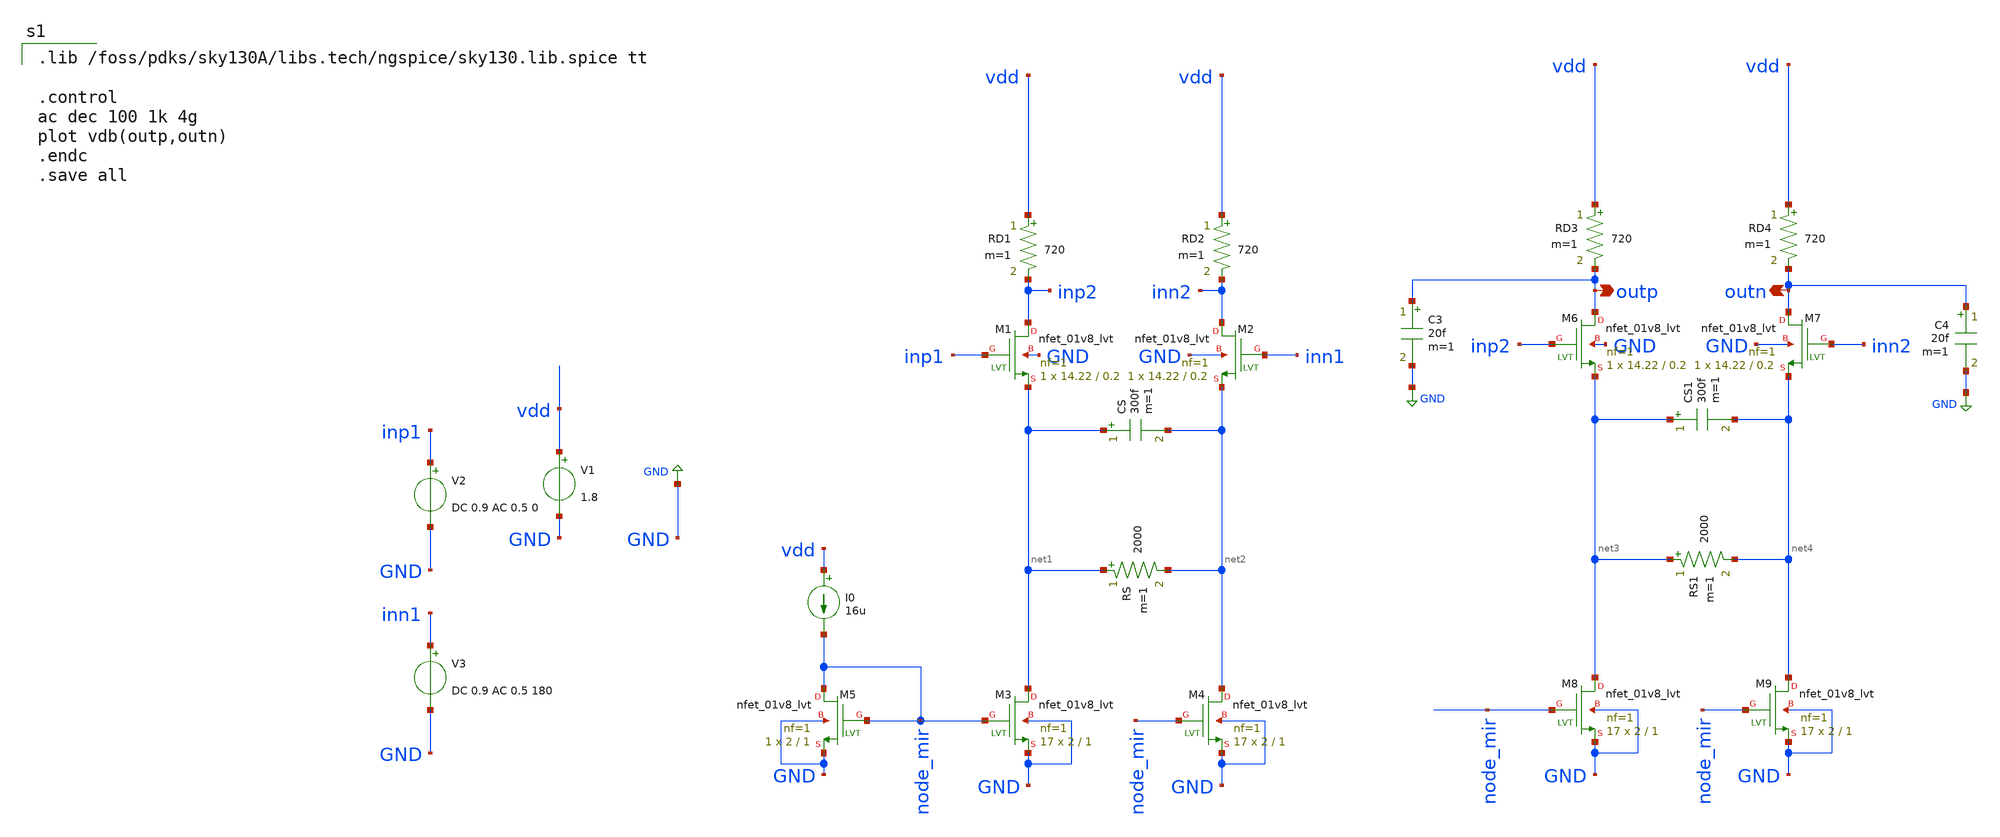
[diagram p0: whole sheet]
** sch_path: CTLE/ctle_two_stage.sch
**.subckt ctle_two_stage outp outn
*.opin outp
*.opin outn
V1 vdd GND 1.8
V2 inp1 GND DC 0.9 AC 0.5 0
V3 inn1 GND DC 0.9 AC 0.5 180
XM1 inp2 inp1 net1 GND sky130_fd_pr__nfet_01v8_lvt L=0.2 W=14.22 nf=1 ad='int((nf+1)/2) * W/nf * 0.29'
+ as='int((nf+2)/2) * W/nf * 0.29' pd='2*int((nf+1)/2) * (W/nf + 0.29)' ps='2*int((nf+2)/2) * (W/nf + 0.29)'
+ nrd='0.29 / W' nrs='0.29 / W' sa=0 sb=0 sd=0 mult=1 m=1
XM2 inn2 inn1 net2 GND sky130_fd_pr__nfet_01v8_lvt L=0.2 W=14.22 nf=1 ad='int((nf+1)/2) * W/nf * 0.29'
+ as='int((nf+2)/2) * W/nf * 0.29' pd='2*int((nf+1)/2) * (W/nf + 0.29)' ps='2*int((nf+2)/2) * (W/nf + 0.29)'
+ nrd='0.29 / W' nrs='0.29 / W' sa=0 sb=0 sd=0 mult=1 m=1
I0 vdd node_mir 16u
XM3 net1 node_mir GND GND sky130_fd_pr__nfet_01v8_lvt L=1 W=2 nf=1 ad='int((nf+1)/2) * W/nf * 0.29' as='int((nf+2)/2) * W/nf * 0.29'
+ pd='2*int((nf+1)/2) * (W/nf + 0.29)' ps='2*int((nf+2)/2) * (W/nf + 0.29)' nrd='0.29 / W' nrs='0.29 / W'
+ sa=0 sb=0 sd=0 mult=17 m=17
XM4 net2 node_mir GND GND sky130_fd_pr__nfet_01v8_lvt L=1 W=2 nf=1 ad='int((nf+1)/2) * W/nf * 0.29' as='int((nf+2)/2) * W/nf * 0.29'
+ pd='2*int((nf+1)/2) * (W/nf + 0.29)' ps='2*int((nf+2)/2) * (W/nf + 0.29)' nrd='0.29 / W' nrs='0.29 / W'
+ sa=0 sb=0 sd=0 mult=17 m=17
XM5 node_mir node_mir GND GND sky130_fd_pr__nfet_01v8_lvt L=1 W=2 nf=1 ad='int((nf+1)/2) * W/nf * 0.29'
+ as='int((nf+2)/2) * W/nf * 0.29' pd='2*int((nf+1)/2) * (W/nf + 0.29)' ps='2*int((nf+2)/2) * (W/nf + 0.29)'
+ nrd='0.29 / W' nrs='0.29 / W' sa=0 sb=0 sd=0 mult=1 m=1
RD1 vdd inp2 720 m=1
RD2 vdd inn2 720 m=1
CS net1 net2 300f m=1
RS net1 net2 2000 m=1
XM6 outp inp2 net3 GND sky130_fd_pr__nfet_01v8_lvt L=0.2 W=14.22 nf=1 ad='int((nf+1)/2) * W/nf * 0.29'
+ as='int((nf+2)/2) * W/nf * 0.29' pd='2*int((nf+1)/2) * (W/nf + 0.29)' ps='2*int((nf+2)/2) * (W/nf + 0.29)'
+ nrd='0.29 / W' nrs='0.29 / W' sa=0 sb=0 sd=0 mult=1 m=1
XM7 outn inn2 net4 GND sky130_fd_pr__nfet_01v8_lvt L=0.2 W=14.22 nf=1 ad='int((nf+1)/2) * W/nf * 0.29'
+ as='int((nf+2)/2) * W/nf * 0.29' pd='2*int((nf+1)/2) * (W/nf + 0.29)' ps='2*int((nf+2)/2) * (W/nf + 0.29)'
+ nrd='0.29 / W' nrs='0.29 / W' sa=0 sb=0 sd=0 mult=1 m=1
XM8 net3 node_mir GND GND sky130_fd_pr__nfet_01v8_lvt L=1 W=2 nf=1 ad='int((nf+1)/2) * W/nf * 0.29' as='int((nf+2)/2) * W/nf * 0.29'
+ pd='2*int((nf+1)/2) * (W/nf + 0.29)' ps='2*int((nf+2)/2) * (W/nf + 0.29)' nrd='0.29 / W' nrs='0.29 / W'
+ sa=0 sb=0 sd=0 mult=17 m=17
XM9 net4 node_mir GND GND sky130_fd_pr__nfet_01v8_lvt L=1 W=2 nf=1 ad='int((nf+1)/2) * W/nf * 0.29' as='int((nf+2)/2) * W/nf * 0.29'
+ pd='2*int((nf+1)/2) * (W/nf + 0.29)' ps='2*int((nf+2)/2) * (W/nf + 0.29)' nrd='0.29 / W' nrs='0.29 / W'
+ sa=0 sb=0 sd=0 mult=17 m=17
RD3 vdd outp 720 m=1
RD4 vdd outn 720 m=1
CS1 net3 net4 300f m=1
RS1 net3 net4 2000 m=1
C3 outp GND 20f m=1
C4 outn GND 20f m=1
**** begin user architecture code

.lib /foss/pdks/sky130A/libs.tech/ngspice/sky130.lib.spice tt

.control
ac dec 100 1k 4g
plot vdb(outp,outn)
.endc
.save all


**** end user architecture code
**.ends
.GLOBAL GND
.end
